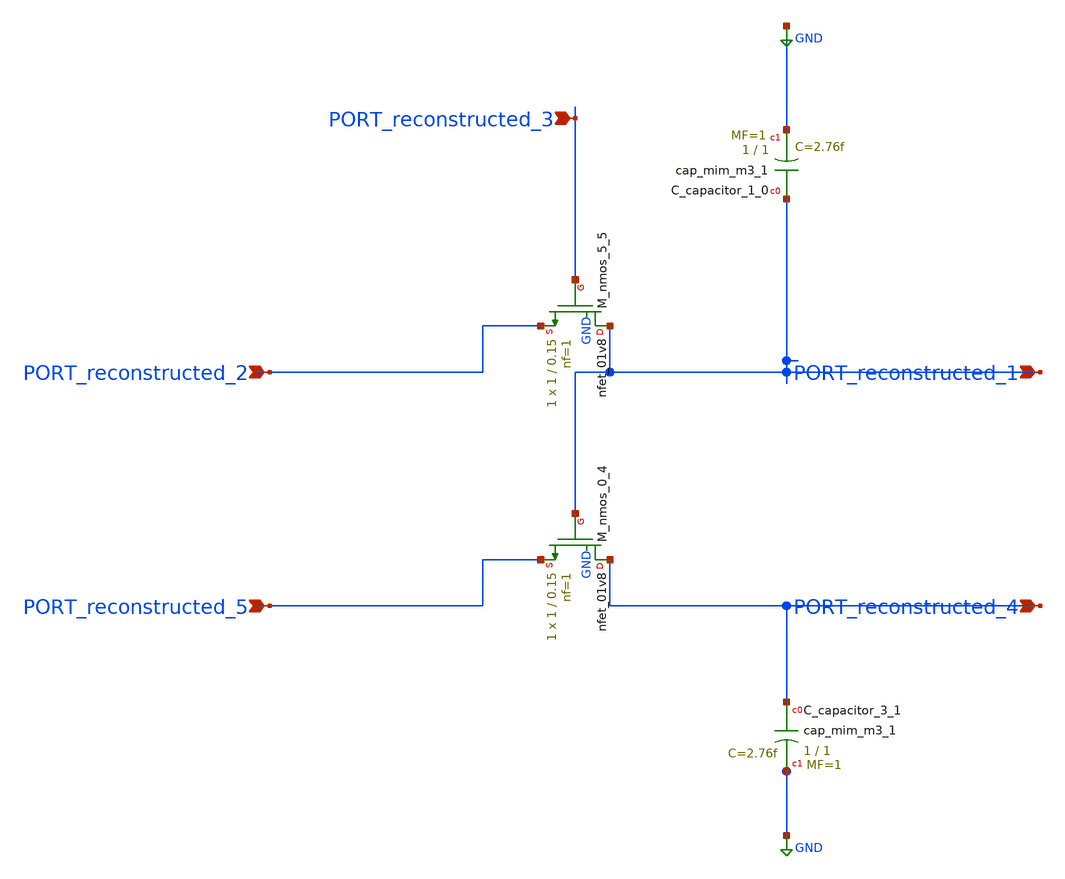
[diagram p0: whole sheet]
** sch_path: schematics/AMSNet/787.sch
**.subckt 787 PORT_reconstructed_3 PORT_reconstructed_4 PORT_reconstructed_5 PORT_reconstructed_1
*+ PORT_reconstructed_2
*.ipin PORT_reconstructed_3
*.ipin PORT_reconstructed_4
*.ipin PORT_reconstructed_5
*.ipin PORT_reconstructed_1
*.ipin PORT_reconstructed_2
XC_capacitor_1_0 PORT_reconstructed_1 GND sky130_fd_pr__cap_mim_m3_1 W=1 L=1 MF=1 m=1
XC_capacitor_3_1 PORT_reconstructed_4 GND sky130_fd_pr__cap_mim_m3_1 W=1 L=1 MF=1 m=1
XM_nmos_0_4 PORT_reconstructed_4 PORT_reconstructed_1 PORT_reconstructed_5 GND sky130_fd_pr__nfet_01v8
+ L=0.15 W=1 nf=1 ad='int((1 + 1)/2) * 1 / 1 * 0.29' as='int((1 + 2)/2) * 1 / 1 * 0.29' pd='2*int((1 + 1)/2) * (1 / 1 + 0.29)'
+ ps='2*int((1 + 2)/2) * (1 / 1 + 0.29)' nrd='0.29 / 1 ' nrs='0.29 / 1 ' sa=0 sb=0 sd=0 mult=1 m=1
XM_nmos_5_5 PORT_reconstructed_1 PORT_reconstructed_3 PORT_reconstructed_2 GND sky130_fd_pr__nfet_01v8
+ L=0.15 W=1 nf=1 ad='int((1 + 1)/2) * 1 / 1 * 0.29' as='int((1 + 2)/2) * 1 / 1 * 0.29' pd='2*int((1 + 1)/2) * (1 / 1 + 0.29)'
+ ps='2*int((1 + 2)/2) * (1 / 1 + 0.29)' nrd='0.29 / 1 ' nrs='0.29 / 1 ' sa=0 sb=0 sd=0 mult=1 m=1
**.ends
.GLOBAL GND
.end
